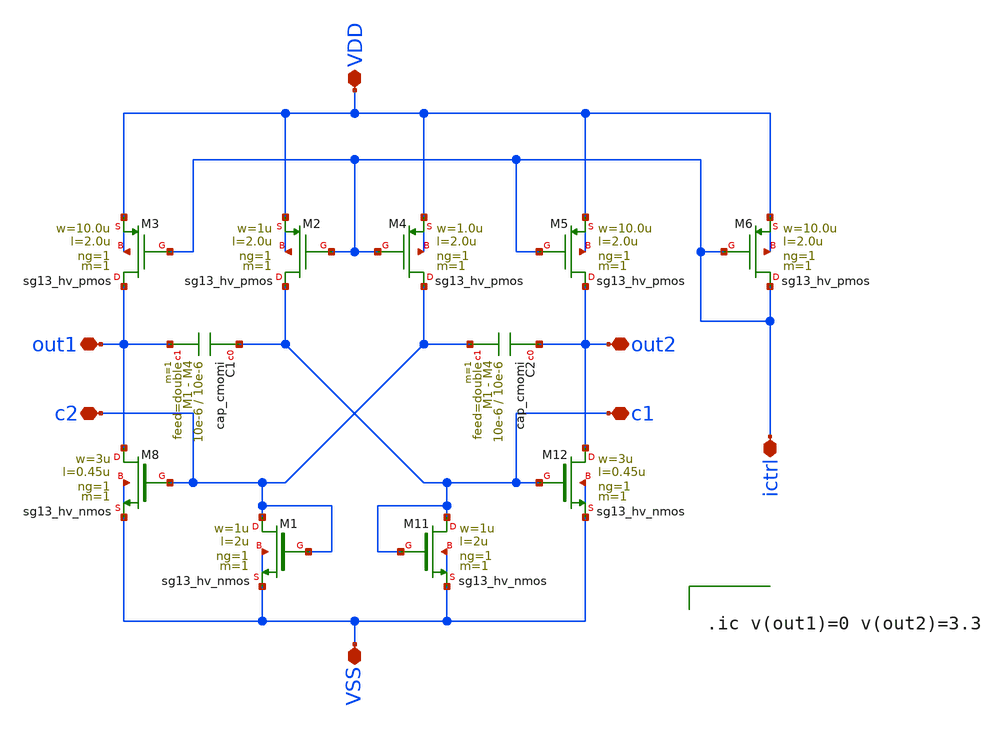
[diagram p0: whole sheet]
** sch_path: macros/heichips26_vcr/macros/switched_capacitor/schematic/xschem/osc_wcap.sch
**.subckt osc_wcap VSS VDD out2 out1 c2 ictrl c1
*.iopin VSS
*.iopin VDD
*.iopin out2
*.iopin out1
*.iopin c2
*.iopin ictrl
*.iopin c1
XM3 out1 ictrl VDD VDD sg13_hv_pmos w=10.0u l=2.0u ng=1 m=1 mm_ok=1
XM2 c1 ictrl VDD VDD sg13_hv_pmos w=1u l=2.0u ng=1 m=1 mm_ok=1
XM4 c2 ictrl VDD VDD sg13_hv_pmos w=1.0u l=2.0u ng=1 m=1 mm_ok=1
XM5 out2 ictrl VDD VDD sg13_hv_pmos w=10.0u l=2.0u ng=1 m=1 mm_ok=1
XM6 ictrl ictrl VDD VDD sg13_hv_pmos w=10.0u l=2.0u ng=1 m=1 mm_ok=1
XC1 c1 out1 cap_cmomi w=10e-6 l=10e-6 mmin=1 mmax=4 feed=double subblock=0 m=1 mm_ok=1
XC2 out2 c2 cap_cmomi w=10e-6 l=10e-6 mmin=1 mmax=4 feed=double subblock=0 m=1 mm_ok=1
XM8 out1 c2 VSS VSS sg13_hv_nmos w=3u l=0.45u ng=1 m=1 mm_ok=1
XM1 c2 c2 VSS VSS sg13_hv_nmos w=1u l=2u ng=1 m=1 mm_ok=1
XM12 out2 c1 VSS VSS sg13_hv_nmos w=3u l=0.45u ng=1 m=1 mm_ok=1
XM11 c1 c1 VSS VSS sg13_hv_nmos w=1u l=2u ng=1 m=1 mm_ok=1
**** begin user architecture code


.ic v(out1)=0 v(out2)=3.3


**** end user architecture code
**.ends
.end
